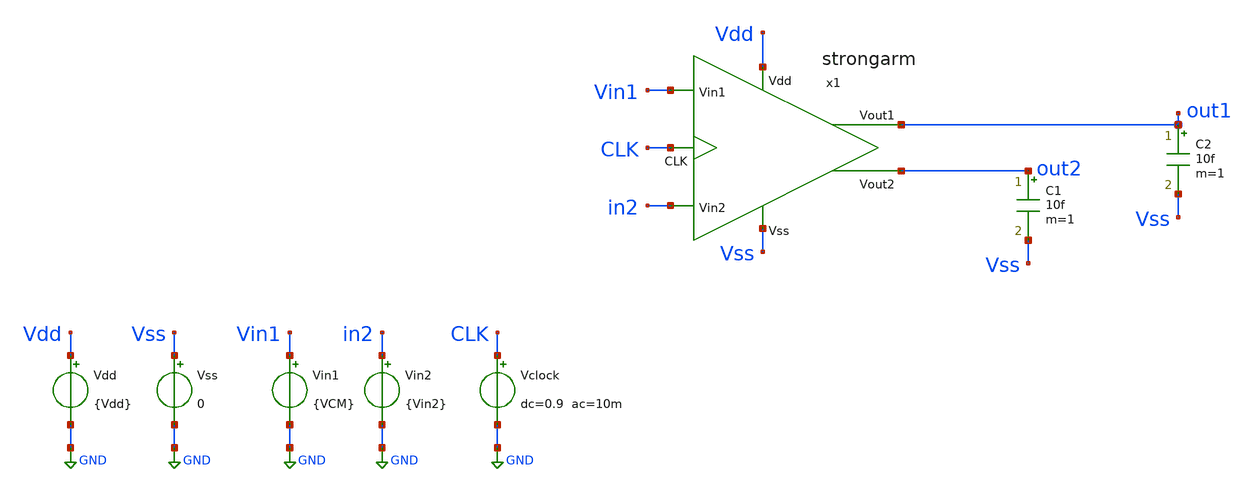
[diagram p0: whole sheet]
** sch_path: xschem/TB/TB_Op_SA.sch
**.subckt TB_Op_SA
Vdd Vdd GND {Vdd}
x1 out2 out1 Vdd Vss in2 Vin1 CLK strongarm
Vss Vss GND 0
C1 out2 Vss 10f m=1
C2 out1 Vss 10f m=1
Vin1 Vin1 GND {VCM}
Vin2 in2 GND {Vin2}
Vclock CLK GND dc=0.9 ac=10m
**** begin user architecture code


.control
save all  @n.x1.xm3.nsg13_lv_nmos[gm]  @n.x1.xm4.nsg13_lv_nmos[gm]  @n.x1.xm3.nsg13_lv_nmos[ids]
+  @n.x1.xm4.nsg13_lv_nmos[ids]
*  @n.x1.xm8.nsg13_lv_pmos[ids]
op
let id3 = @n.x1.xm3.nsg13_lv_nmos[ids]
let id4 = @n.x1.xm4.nsg13_lv_nmos[ids]
let id8 = @n.x1.xm8.nsg13_lv_pmos[ids]

let gm3 = @n.x1.xm3.nsg13_lv_nmos[gm]
let gm4 = @n.x1.xm4.nsg13_lv_nmos[gm]
print id8 id3 id4
print gm3 gm4
.endc




.param Vdd   = 1.8
.param VCM   = 0.9
.param Vstep = 10m
.param Vin2  = VCM-Vstep
.ic V(out1) = 1.8
.ic V(out2) = 1.8
.ic V(x1.common) = 1.8
.ic V(x1.P) = 1.8
.ic V(x1.Q) = 1.8





.lib cornerMOSlv.lib mos_tt




** TRANSISTORES NMOS

.param W12 = 0.5u
.param L12 = 0.13u
.param M12 = 10

.param W34 = 0.5u
.param L34 = 0.13u
.param M34 = 5

.param W56 = 0.5u
.param L56 = 0.13u
.param M56 = 5

.param W7  = 0.5u
.param L7  = 0.13u
.param M7  = 20

.param W89 = 0.5u
.param L89 = 0.13u
.param M89 = 1

.param Wab = 0.5u
.param Lab = 0.13u
.param Mab = 3


**** end user architecture code
**.ends

* expanding   symbol:  ../sch/strongarm.sym # of pins=7
** sym_path: xschem/sch/strongarm.sym
** sch_path: xschem/sch/strongarm.sch
.subckt strongarm Vout2 Vout1 Vdd Vss Vin2 Vin1 CLK
*.opin Vout2
*.opin Vout1
*.ipin Vin1
*.ipin Vin2
*.ipin CLK
*.ipin Vss
*.ipin Vdd
XM1 common Vin1 P Vss sg13_lv_nmos w={W12} l={L12} ng=1 m={M12} mm_ok=1
XM2 common Vin2 Q Vss sg13_lv_nmos w={W12} l={L12} ng=1 m={M12} mm_ok=1
XM3 P Vout2 Vout1 Vss sg13_lv_nmos w={W34} l={L34} ng=1 m={M34} mm_ok=1
XM4 Q Vout1 Vout2 Vss sg13_lv_nmos w={W34} l={L34} ng=1 m={M34} mm_ok=1
XM6 Vout2 Vout1 Vdd Vdd sg13_lv_pmos w={W56} l={L56} ng=1 m={M56} mm_ok=1
XM5 Vout1 Vout2 Vdd Vdd sg13_lv_pmos w={W56} l={L56} ng=1 m={M56} mm_ok=1
XM7 Vss CLK common Vss sg13_lv_nmos w={W7} l={L7} ng=1 m={M7} mm_ok=1
XM8 P CLK Vdd Vdd sg13_lv_pmos w={W89} l={L89} ng=1 m={M89} mm_ok=1
XM9 Q CLK Vdd Vdd sg13_lv_pmos w={W89} l={L89} ng=1 m={M89} mm_ok=1
XM11 Vdd CLK Vout2 Vdd sg13_lv_pmos w={Wab} l={Lab} ng=1 m={Mab} mm_ok=1
XM10 Vdd CLK Vout1 Vdd sg13_lv_pmos w={Wab} l={Lab} ng=1 m={Mab} mm_ok=1
.ends

.GLOBAL GND
.end
